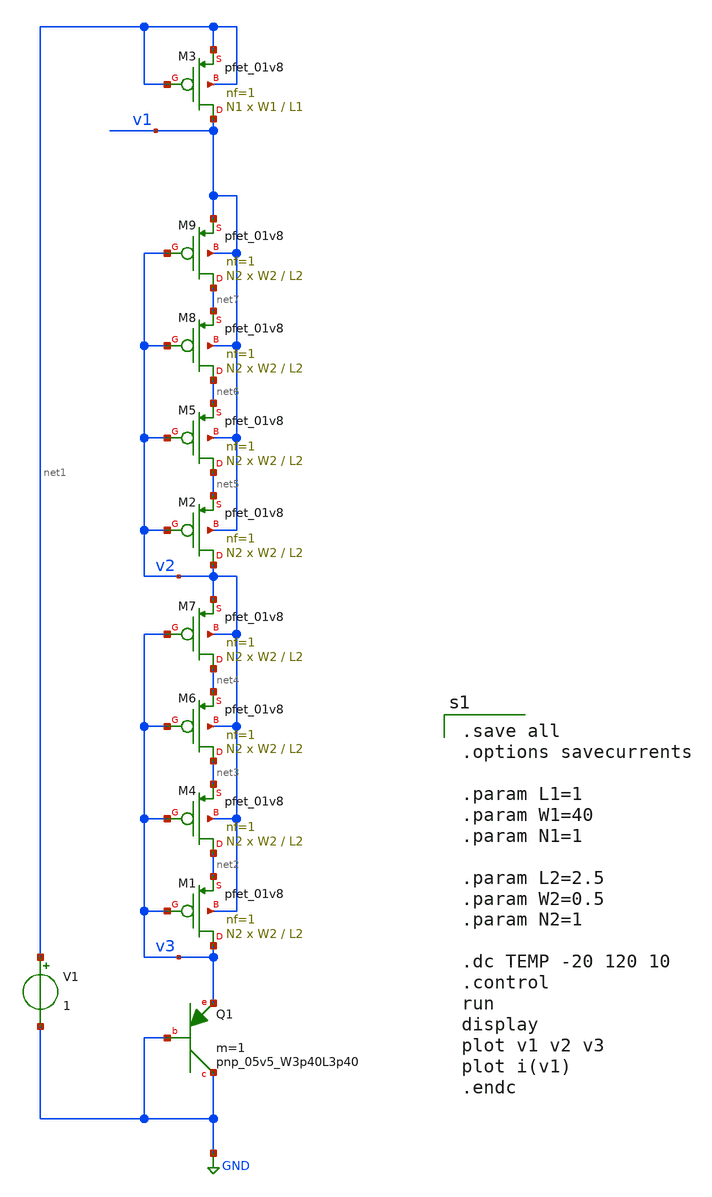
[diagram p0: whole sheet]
** sch_path: SKY130/xschem/cmos_vref/Y.Ji_JSSC2019/s2_ztat.sch
**.subckt s2_ztat
XQ1 GND GND v3 sky130_fd_pr__pnp_05v5_W3p40L3p40 m=1
V1 net1 GND 1
XM3 v1 net1 net1 net1 sky130_fd_pr__pfet_01v8 L=L1 W=W1 nf=1 ad='int((nf+1)/2) * W/nf * 0.29' as='int((nf+2)/2) * W/nf * 0.29'
+ pd='2*int((nf+1)/2) * (W/nf + 0.29)' ps='2*int((nf+2)/2) * (W/nf + 0.29)' nrd='0.29 / W' nrs='0.29 / W'
+ sa=0 sb=0 sd=0 mult=N1 m=N1
XM1 v3 v3 net2 v2 sky130_fd_pr__pfet_01v8 L=L2 W=W2 nf=1 ad='int((nf+1)/2) * W/nf * 0.29' as='int((nf+2)/2) * W/nf * 0.29'
+ pd='2*int((nf+1)/2) * (W/nf + 0.29)' ps='2*int((nf+2)/2) * (W/nf + 0.29)' nrd='0.29 / W' nrs='0.29 / W'
+ sa=0 sb=0 sd=0 mult=N2 m=N2
XM4 net2 v3 net3 v2 sky130_fd_pr__pfet_01v8 L=L2 W=W2 nf=1 ad='int((nf+1)/2) * W/nf * 0.29' as='int((nf+2)/2) * W/nf * 0.29'
+ pd='2*int((nf+1)/2) * (W/nf + 0.29)' ps='2*int((nf+2)/2) * (W/nf + 0.29)' nrd='0.29 / W' nrs='0.29 / W'
+ sa=0 sb=0 sd=0 mult=N2 m=N2
XM6 net3 v3 net4 v2 sky130_fd_pr__pfet_01v8 L=L2 W=W2 nf=1 ad='int((nf+1)/2) * W/nf * 0.29' as='int((nf+2)/2) * W/nf * 0.29'
+ pd='2*int((nf+1)/2) * (W/nf + 0.29)' ps='2*int((nf+2)/2) * (W/nf + 0.29)' nrd='0.29 / W' nrs='0.29 / W'
+ sa=0 sb=0 sd=0 mult=N2 m=N2
XM7 net4 v3 v2 v2 sky130_fd_pr__pfet_01v8 L=L2 W=W2 nf=1 ad='int((nf+1)/2) * W/nf * 0.29' as='int((nf+2)/2) * W/nf * 0.29'
+ pd='2*int((nf+1)/2) * (W/nf + 0.29)' ps='2*int((nf+2)/2) * (W/nf + 0.29)' nrd='0.29 / W' nrs='0.29 / W'
+ sa=0 sb=0 sd=0 mult=N2 m=N2
XM2 v2 v2 net5 v1 sky130_fd_pr__pfet_01v8 L=L2 W=W2 nf=1 ad='int((nf+1)/2) * W/nf * 0.29' as='int((nf+2)/2) * W/nf * 0.29'
+ pd='2*int((nf+1)/2) * (W/nf + 0.29)' ps='2*int((nf+2)/2) * (W/nf + 0.29)' nrd='0.29 / W' nrs='0.29 / W'
+ sa=0 sb=0 sd=0 mult=N2 m=N2
XM5 net5 v2 net6 v1 sky130_fd_pr__pfet_01v8 L=L2 W=W2 nf=1 ad='int((nf+1)/2) * W/nf * 0.29' as='int((nf+2)/2) * W/nf * 0.29'
+ pd='2*int((nf+1)/2) * (W/nf + 0.29)' ps='2*int((nf+2)/2) * (W/nf + 0.29)' nrd='0.29 / W' nrs='0.29 / W'
+ sa=0 sb=0 sd=0 mult=N2 m=N2
XM8 net6 v2 net7 v1 sky130_fd_pr__pfet_01v8 L=L2 W=W2 nf=1 ad='int((nf+1)/2) * W/nf * 0.29' as='int((nf+2)/2) * W/nf * 0.29'
+ pd='2*int((nf+1)/2) * (W/nf + 0.29)' ps='2*int((nf+2)/2) * (W/nf + 0.29)' nrd='0.29 / W' nrs='0.29 / W'
+ sa=0 sb=0 sd=0 mult=N2 m=N2
XM9 net7 v2 v1 v1 sky130_fd_pr__pfet_01v8 L=L2 W=W2 nf=1 ad='int((nf+1)/2) * W/nf * 0.29' as='int((nf+2)/2) * W/nf * 0.29'
+ pd='2*int((nf+1)/2) * (W/nf + 0.29)' ps='2*int((nf+2)/2) * (W/nf + 0.29)' nrd='0.29 / W' nrs='0.29 / W'
+ sa=0 sb=0 sd=0 mult=N2 m=N2
**** begin user architecture code
.lib $::SKYWATER_MODELS/sky130.lib.spice tt
.include $::PDKPATH/libs.ref/sky130_fd_sc_hvl/spice/sky130_fd_sc_hvl.spice

.save all
.options savecurrents

.param L1=1
.param W1=40
.param N1=1

.param L2=2.5
.param W2=0.5
.param N2=1

.dc TEMP -20 120 10
.control
run
display
plot v1 v2 v3
plot i(v1)
.endc


**** end user architecture code
**.ends
.GLOBAL GND
.end
